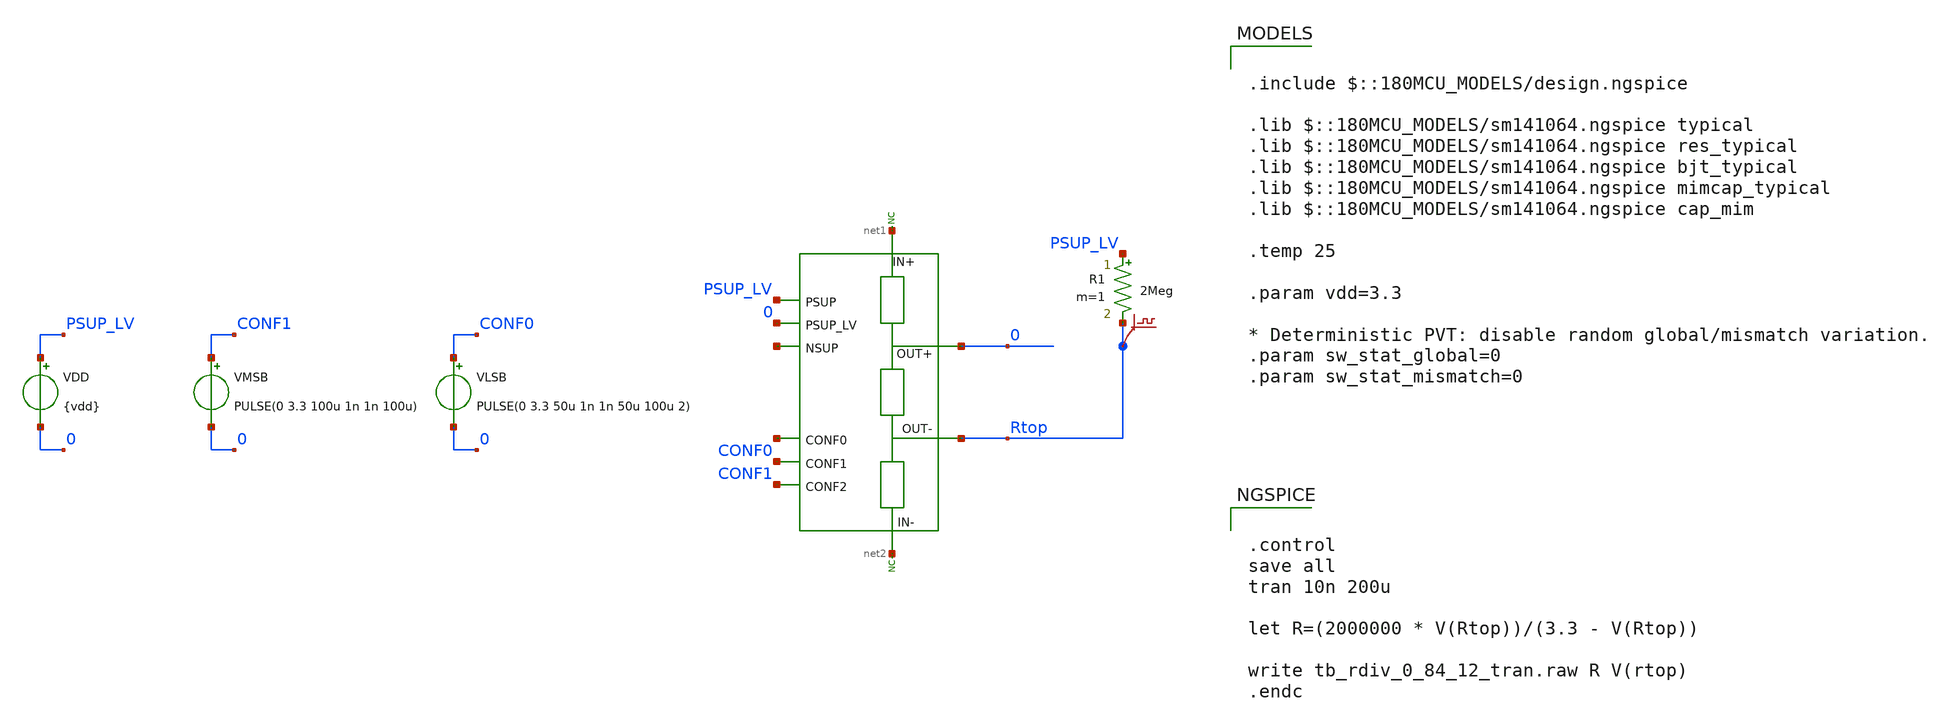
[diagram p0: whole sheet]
** sch_path: xschem/blocks/INA_gain_fb/tb_INA_gain_fb_tran.sch
**.subckt tb_INA_gain_fb_tran
VLSB CONF0 0 PULSE(0 3.3 50u 1n 1n 50u 100u 2)
VMSB CONF1 0 PULSE(0 3.3 100u 1n 1n 100u)
VDD PSUP_LV 0 {vdd}
* noconn #net2
* noconn #net1
R1 PSUP_LV Rtop 2Meg m=1
.save v(rtop)
**** begin user architecture code

.include $::180MCU_MODELS/design.ngspice

.lib $::180MCU_MODELS/sm141064.ngspice typical
.lib $::180MCU_MODELS/sm141064.ngspice res_typical
.lib $::180MCU_MODELS/sm141064.ngspice bjt_typical
.lib $::180MCU_MODELS/sm141064.ngspice mimcap_typical
.lib $::180MCU_MODELS/sm141064.ngspice cap_mim

.temp 25

.param vdd=3.3

* Deterministic PVT: disable random global/mismatch variation.
.param sw_stat_global=0
.param sw_stat_mismatch=0



.control
save all
tran 10n 200u

let R=(2000000 * V(Rtop))/(3.3 - V(Rtop))

write tb_rdiv_0_84_12_tran.raw R V(rtop)
.endc


**** end user architecture code
**.ends
.end
